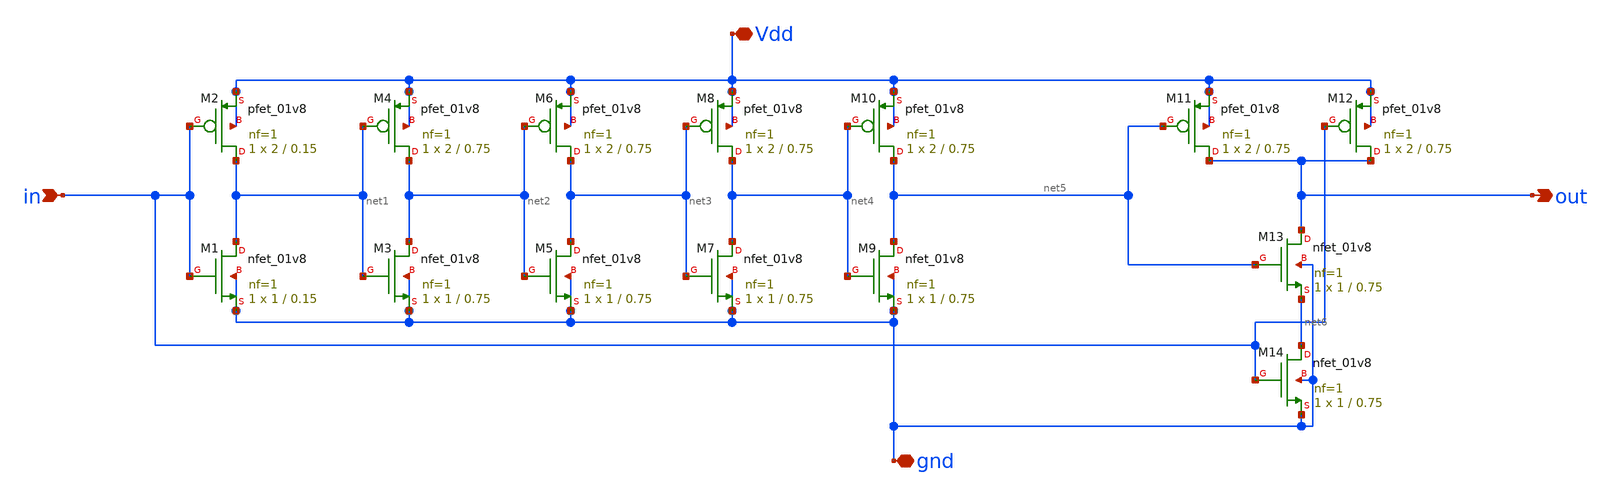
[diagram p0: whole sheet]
** sch_path: xschem/pulse_generator.sch
**.subckt pulse_generator Vdd in out gnd
*.iopin Vdd
*.ipin in
*.opin out
*.iopin gnd
XM1 net1 in gnd gnd sky130_fd_pr__nfet_01v8 L=0.15 W=1 nf=1 ad='int((nf+1)/2) * W/nf * 0.29' as='int((nf+2)/2) * W/nf * 0.29'
+ pd='2*int((nf+1)/2) * (W/nf + 0.29)' ps='2*int((nf+2)/2) * (W/nf + 0.29)' nrd='0.29 / W' nrs='0.29 / W'
+ sa=0 sb=0 sd=0 mult=1 m=1
XM3 net2 net1 gnd gnd sky130_fd_pr__nfet_01v8 L=0.75 W=1 nf=1 ad='int((nf+1)/2) * W/nf * 0.29' as='int((nf+2)/2) * W/nf * 0.29'
+ pd='2*int((nf+1)/2) * (W/nf + 0.29)' ps='2*int((nf+2)/2) * (W/nf + 0.29)' nrd='0.29 / W' nrs='0.29 / W'
+ sa=0 sb=0 sd=0 mult=1 m=1
XM5 net3 net2 gnd gnd sky130_fd_pr__nfet_01v8 L=0.75 W=1 nf=1 ad='int((nf+1)/2) * W/nf * 0.29' as='int((nf+2)/2) * W/nf * 0.29'
+ pd='2*int((nf+1)/2) * (W/nf + 0.29)' ps='2*int((nf+2)/2) * (W/nf + 0.29)' nrd='0.29 / W' nrs='0.29 / W'
+ sa=0 sb=0 sd=0 mult=1 m=1
XM7 net4 net3 gnd gnd sky130_fd_pr__nfet_01v8 L=0.75 W=1 nf=1 ad='int((nf+1)/2) * W/nf * 0.29' as='int((nf+2)/2) * W/nf * 0.29'
+ pd='2*int((nf+1)/2) * (W/nf + 0.29)' ps='2*int((nf+2)/2) * (W/nf + 0.29)' nrd='0.29 / W' nrs='0.29 / W'
+ sa=0 sb=0 sd=0 mult=1 m=1
XM9 net5 net4 gnd gnd sky130_fd_pr__nfet_01v8 L=0.75 W=1 nf=1 ad='int((nf+1)/2) * W/nf * 0.29' as='int((nf+2)/2) * W/nf * 0.29'
+ pd='2*int((nf+1)/2) * (W/nf + 0.29)' ps='2*int((nf+2)/2) * (W/nf + 0.29)' nrd='0.29 / W' nrs='0.29 / W'
+ sa=0 sb=0 sd=0 mult=1 m=1
XM13 out net5 net6 gnd sky130_fd_pr__nfet_01v8 L=0.75 W=1 nf=1 ad='int((nf+1)/2) * W/nf * 0.29' as='int((nf+2)/2) * W/nf * 0.29'
+ pd='2*int((nf+1)/2) * (W/nf + 0.29)' ps='2*int((nf+2)/2) * (W/nf + 0.29)' nrd='0.29 / W' nrs='0.29 / W'
+ sa=0 sb=0 sd=0 mult=1 m=1
XM14 net6 in gnd gnd sky130_fd_pr__nfet_01v8 L=0.75 W=1 nf=1 ad='int((nf+1)/2) * W/nf * 0.29' as='int((nf+2)/2) * W/nf * 0.29'
+ pd='2*int((nf+1)/2) * (W/nf + 0.29)' ps='2*int((nf+2)/2) * (W/nf + 0.29)' nrd='0.29 / W' nrs='0.29 / W'
+ sa=0 sb=0 sd=0 mult=1 m=1
XM2 net1 in Vdd Vdd sky130_fd_pr__pfet_01v8 L=0.15 W=2 nf=1 ad='int((nf+1)/2) * W/nf * 0.29' as='int((nf+2)/2) * W/nf * 0.29'
+ pd='2*int((nf+1)/2) * (W/nf + 0.29)' ps='2*int((nf+2)/2) * (W/nf + 0.29)' nrd='0.29 / W' nrs='0.29 / W'
+ sa=0 sb=0 sd=0 mult=1 m=1
XM4 net2 net1 Vdd Vdd sky130_fd_pr__pfet_01v8 L=0.75 W=2 nf=1 ad='int((nf+1)/2) * W/nf * 0.29' as='int((nf+2)/2) * W/nf * 0.29'
+ pd='2*int((nf+1)/2) * (W/nf + 0.29)' ps='2*int((nf+2)/2) * (W/nf + 0.29)' nrd='0.29 / W' nrs='0.29 / W'
+ sa=0 sb=0 sd=0 mult=1 m=1
XM6 net3 net2 Vdd Vdd sky130_fd_pr__pfet_01v8 L=0.75 W=2 nf=1 ad='int((nf+1)/2) * W/nf * 0.29' as='int((nf+2)/2) * W/nf * 0.29'
+ pd='2*int((nf+1)/2) * (W/nf + 0.29)' ps='2*int((nf+2)/2) * (W/nf + 0.29)' nrd='0.29 / W' nrs='0.29 / W'
+ sa=0 sb=0 sd=0 mult=1 m=1
XM8 net4 net3 Vdd Vdd sky130_fd_pr__pfet_01v8 L=0.75 W=2 nf=1 ad='int((nf+1)/2) * W/nf * 0.29' as='int((nf+2)/2) * W/nf * 0.29'
+ pd='2*int((nf+1)/2) * (W/nf + 0.29)' ps='2*int((nf+2)/2) * (W/nf + 0.29)' nrd='0.29 / W' nrs='0.29 / W'
+ sa=0 sb=0 sd=0 mult=1 m=1
XM10 net5 net4 Vdd Vdd sky130_fd_pr__pfet_01v8 L=0.75 W=2 nf=1 ad='int((nf+1)/2) * W/nf * 0.29' as='int((nf+2)/2) * W/nf * 0.29'
+ pd='2*int((nf+1)/2) * (W/nf + 0.29)' ps='2*int((nf+2)/2) * (W/nf + 0.29)' nrd='0.29 / W' nrs='0.29 / W'
+ sa=0 sb=0 sd=0 mult=1 m=1
XM11 out net5 Vdd Vdd sky130_fd_pr__pfet_01v8 L=0.75 W=2 nf=1 ad='int((nf+1)/2) * W/nf * 0.29' as='int((nf+2)/2) * W/nf * 0.29'
+ pd='2*int((nf+1)/2) * (W/nf + 0.29)' ps='2*int((nf+2)/2) * (W/nf + 0.29)' nrd='0.29 / W' nrs='0.29 / W'
+ sa=0 sb=0 sd=0 mult=1 m=1
XM12 out in Vdd Vdd sky130_fd_pr__pfet_01v8 L=0.75 W=2 nf=1 ad='int((nf+1)/2) * W/nf * 0.29' as='int((nf+2)/2) * W/nf * 0.29'
+ pd='2*int((nf+1)/2) * (W/nf + 0.29)' ps='2*int((nf+2)/2) * (W/nf + 0.29)' nrd='0.29 / W' nrs='0.29 / W'
+ sa=0 sb=0 sd=0 mult=1 m=1
**.ends
.end
